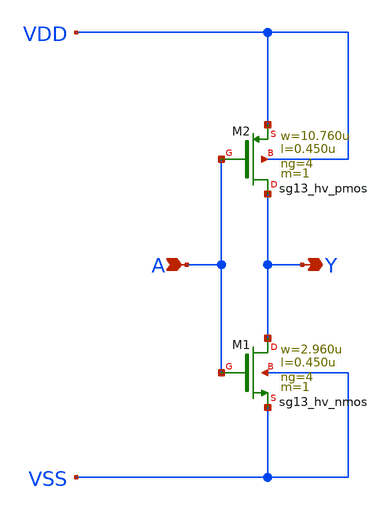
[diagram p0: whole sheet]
** sch_path: ihp-sg13g2/libs.ref/sg13g2_stdcell_hv/sch/xschem/sg13g2_hv_inv_4.sch
* Copyright 2023 IHP PDK Authors
* Licensed under the Apache License, Version 2.0 (the "License");
* you may not use this file except in compliance with the License.
* You may obtain a copy of the License at
* https://www.apache.org/licenses/LICENSE-2.0
* Unless required by applicable law or agreed to in writing, software
* distributed under the License is distributed on an "AS IS" BASIS,
* WITHOUT WARRANTIES OR CONDITIONS OF ANY KIND, either express or implied.
* See the License for the specific language governing permissions and
* limitations under the License.
**.subckt sg13g2_hv_inv_4 A Y
*.ipin A
*.opin Y
XM1 Y A VSS VSS sg13_hv_nmos w=2.960u l=0.450u ng=4 m=1 mm_ok=1
XM2 Y A VDD VDD sg13_hv_pmos w=10.760u l=0.450u ng=4 m=1 mm_ok=1
**.ends
.end
